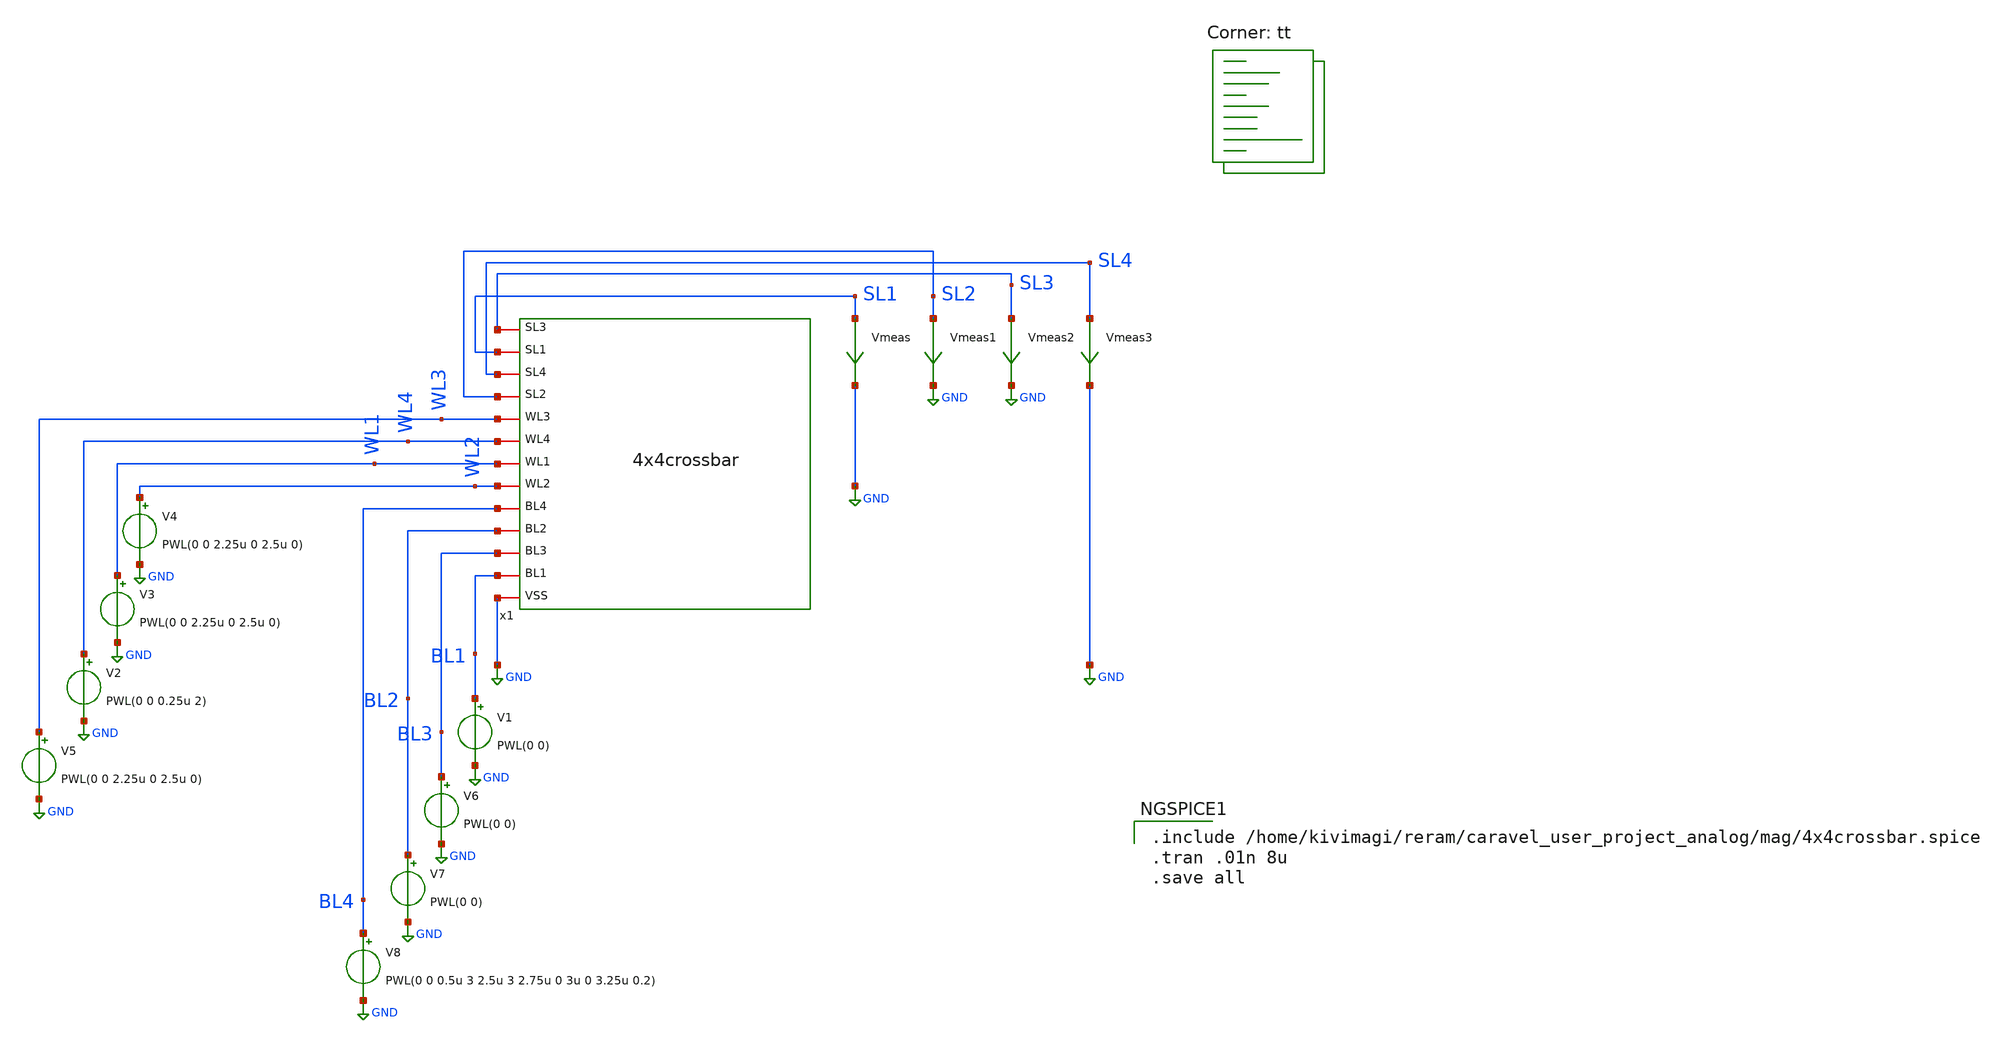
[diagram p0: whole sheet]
** sch_path: xschem/Crossbar/4x4TB.sch
**.subckt 4x4TB
x1 GND BL1 BL3 BL2 BL4 WL2 WL1 WL4 WL3 SL2 SL4 SL1 SL3 4x4crossbar
Vmeas SL1 GND 0
.save i(vmeas)
Vmeas1 SL2 GND 0
.save i(vmeas1)
Vmeas2 SL3 GND 0
.save i(vmeas2)
Vmeas3 SL4 GND 0
.save i(vmeas3)
V1 BL1 GND PWL(0 0)
V5 WL3 GND PWL(0 0 2.25u 0 2.5u 0)
V6 BL3 GND PWL(0 0)
V7 BL2 GND PWL(0 0)
V8 BL4 GND PWL(0 0 0.5u 3 2.5u 3 2.75u 0 3u 0 3.25u 0.2)
V2 WL4 GND PWL(0 0 0.25u 2)
V3 WL1 GND PWL(0 0 2.25u 0 2.5u 0)
V4 WL2 GND PWL(0 0 2.25u 0 2.5u 0)
**** begin user architecture code
.lib $::SKYWATER_MODELS/sky130.lib.spice tt

.include /home/kivimagi/reram/caravel_user_project_analog/mag/4x4crossbar.spice
.tran .01n 8u
.save all


**** end user architecture code
**.ends
.GLOBAL GND
.end
